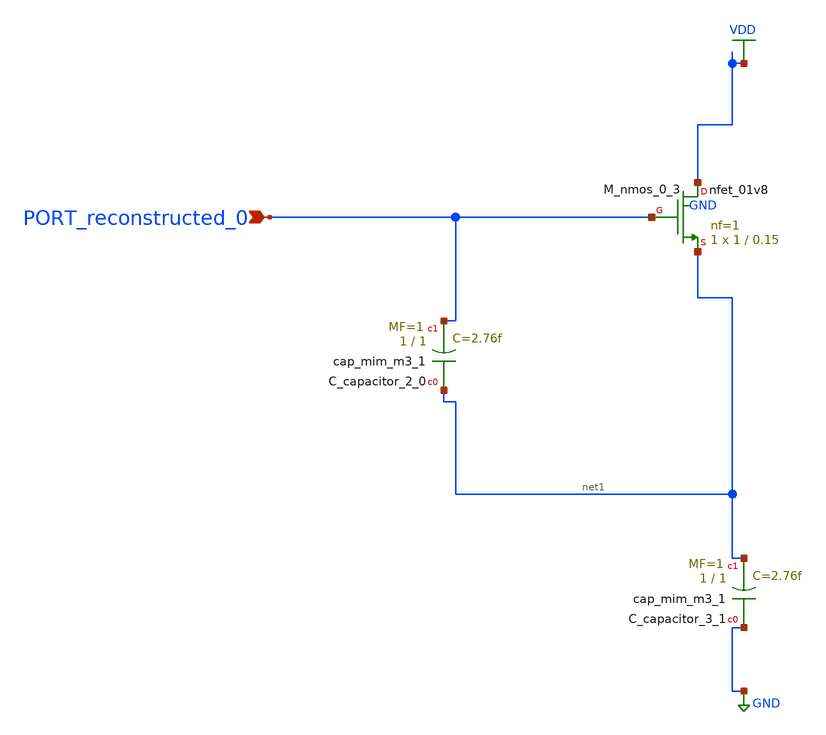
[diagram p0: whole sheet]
** sch_path: schematics/AMSNet/372.sch
**.subckt 372 PORT_reconstructed_0
*.ipin PORT_reconstructed_0
XC_capacitor_2_0 net1 PORT_reconstructed_0 sky130_fd_pr__cap_mim_m3_1 W=1 L=1 MF=1 m=1
XC_capacitor_3_1 GND net1 sky130_fd_pr__cap_mim_m3_1 W=1 L=1 MF=1 m=1
XM_nmos_0_3 VDD PORT_reconstructed_0 net1 GND sky130_fd_pr__nfet_01v8 L=0.15 W=1 nf=1 ad='int((1 + 1)/2) * 1 / 1 * 0.29'
+ as='int((1 + 2)/2) * 1 / 1 * 0.29' pd='2*int((1 + 1)/2) * (1 / 1 + 0.29)' ps='2*int((1 + 2)/2) * (1 / 1 + 0.29)'
+ nrd='0.29 / 1 ' nrs='0.29 / 1 ' sa=0 sb=0 sd=0 mult=1 m=1
**.ends
.GLOBAL GND
.GLOBAL VDD
.end
